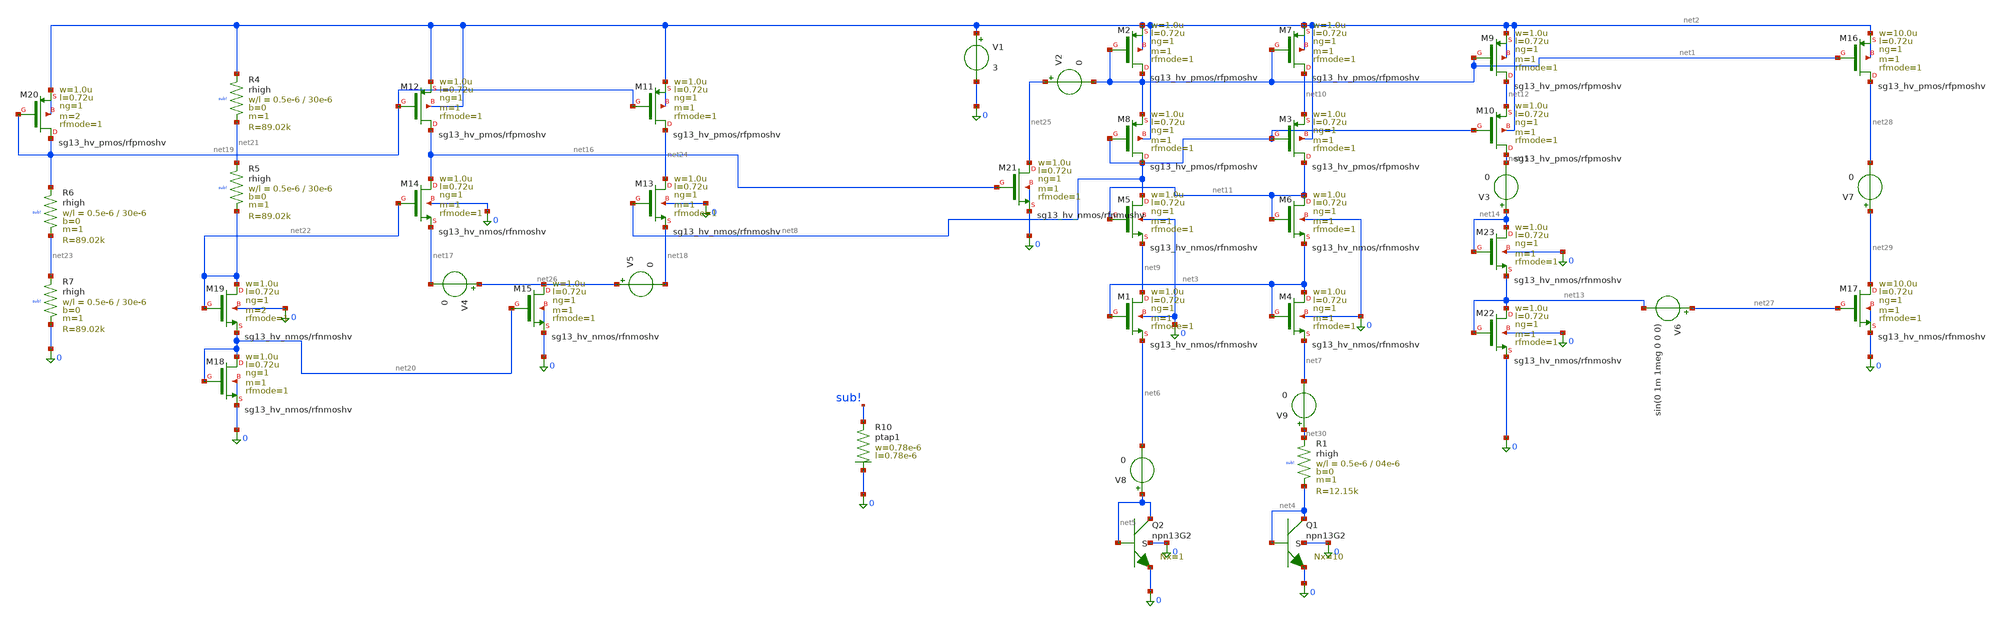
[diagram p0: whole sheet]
** sch_path: src/schematic_op.sch
**.subckt schematic_op
XM8 net8 net8 net1 net2 sg13_hv_pmos w=1.0u l=0.72u ng=1 m=1 rfmode=1 mm_ok=1
XM5 net8 net11 net9 0 sg13_hv_nmos w=1.0u l=0.72u ng=1 m=1 rfmode=1 mm_ok=1
XR1 net30 net4 sub! rhigh w=0.5e-6 l=04e-6 m=1 b=0 mm_ok=1
XM4 net3 net3 net7 0 sg13_hv_nmos w=1.0u l=0.72u ng=1 m=1 rfmode=1 mm_ok=1
XM1 net9 net3 net6 0 sg13_hv_nmos w=1.0u l=0.72u ng=1 m=1 rfmode=1 mm_ok=1
XM7 net10 net1 net2 net2 sg13_hv_pmos w=1.0u l=0.72u ng=1 m=1 rfmode=1 mm_ok=1
XM2 net1 net1 net2 net2 sg13_hv_pmos w=1.0u l=0.72u ng=1 m=1 rfmode=1 mm_ok=1
XQ1 net4 net4 0 0 npn13G2 Nx=10 mm_ok=1
XQ2 net5 net5 0 0 npn13G2 Nx=1 mm_ok=1
XM9 net12 net1 net2 net2 sg13_hv_pmos w=1.0u l=0.72u ng=1 m=1 rfmode=1 mm_ok=1
XM3 net11 net8 net10 net2 sg13_hv_pmos w=1.0u l=0.72u ng=1 m=1 rfmode=1 mm_ok=1
XM6 net11 net11 net3 0 sg13_hv_nmos w=1.0u l=0.72u ng=1 m=1 rfmode=1 mm_ok=1
XM10 net15 net8 net12 net2 sg13_hv_pmos w=1.0u l=0.72u ng=1 m=1 rfmode=1 mm_ok=1
XR10 sub! 0 ptap1 R=262.8 w=0.78e-6 l=0.78e-6
XM22 net13 net13 0 0 sg13_hv_nmos w=1.0u l=0.72u ng=1 m=1 rfmode=1 mm_ok=1
XM23 net14 net14 net13 0 sg13_hv_nmos w=1.0u l=0.72u ng=1 m=1 rfmode=1 mm_ok=1
V1 net2 0 3
V3 net14 net15 0
XM11 net24 net19 net2 net2 sg13_hv_pmos w=1.0u l=0.72u ng=1 m=1 rfmode=1 mm_ok=1
XM12 net16 net19 net2 net2 sg13_hv_pmos w=1.0u l=0.72u ng=1 m=1 rfmode=1 mm_ok=1
XM13 net24 net8 net18 0 sg13_hv_nmos w=1.0u l=0.72u ng=1 m=1 rfmode=1 mm_ok=1
XM14 net16 net22 net17 0 sg13_hv_nmos w=1.0u l=0.72u ng=1 m=1 rfmode=1 mm_ok=1
XM15 net26 net20 0 0 sg13_hv_nmos w=1.0u l=0.72u ng=1 m=1 rfmode=1 mm_ok=1
XM18 net20 net20 0 0 sg13_hv_nmos w=1.0u l=0.72u ng=1 m=1 rfmode=1 mm_ok=1
XM19 net22 net22 net20 0 sg13_hv_nmos w=1.0u l=0.72u ng=1 m=2 rfmode=1 mm_ok=1
XM20 net19 net19 net2 net2 sg13_hv_pmos w=1.0u l=0.72u ng=1 m=2 rfmode=1 mm_ok=1
XR4 net2 net21 sub! rhigh w=0.5e-6 l=30e-6 m=1 b=0 mm_ok=1
XR5 net21 net22 sub! rhigh w=0.5e-6 l=30e-6 m=1 b=0 mm_ok=1
XR6 net19 net23 sub! rhigh w=0.5e-6 l=30e-6 m=1 b=0 mm_ok=1
XR7 net23 0 sub! rhigh w=0.5e-6 l=30e-6 m=1 b=0 mm_ok=1
XM21 net25 net16 0 0 sg13_hv_nmos w=1.0u l=0.72u ng=1 m=1 rfmode=1 mm_ok=1
V2 net25 net1 0
V4 net26 net17 0
V5 net26 net18 0
XM16 net28 net1 net2 net2 sg13_hv_pmos w=10.0u l=0.72u ng=1 m=1 rfmode=1 mm_ok=1
XM17 net29 net27 0 0 sg13_hv_nmos w=10.0u l=0.72u ng=1 m=1 rfmode=1 mm_ok=1
V6 net27 net13 sin(0 1m 1meg 0 0 0)
V7 net29 net28 0
V8 net5 net6 0
V9 net30 net7 0
**** begin user architecture code

.op
.lib cornerMOSlv.lib mos_tt
.lib cornerMOShv.lib mos_tt
.lib cornerHBT.lib hbt_typ
.lib cornerRES.lib res_typ
.lib cornerDIO.lib dio_tt
.param temp=27
.save all
.control
show n.xm17.nsg13_hv_nmos n.xm23.nsg13_hv_nmos n.xm22.nsg13_hv_nmos
show n.xm16.nsg13_hv_pmos n.xm9.nsg13_hv_pmos n.xm10.nsg13_hv_pmos
run
write op_sim.raw
*.options savecurrents
.endc

**** end user architecture code
**.ends
.end
